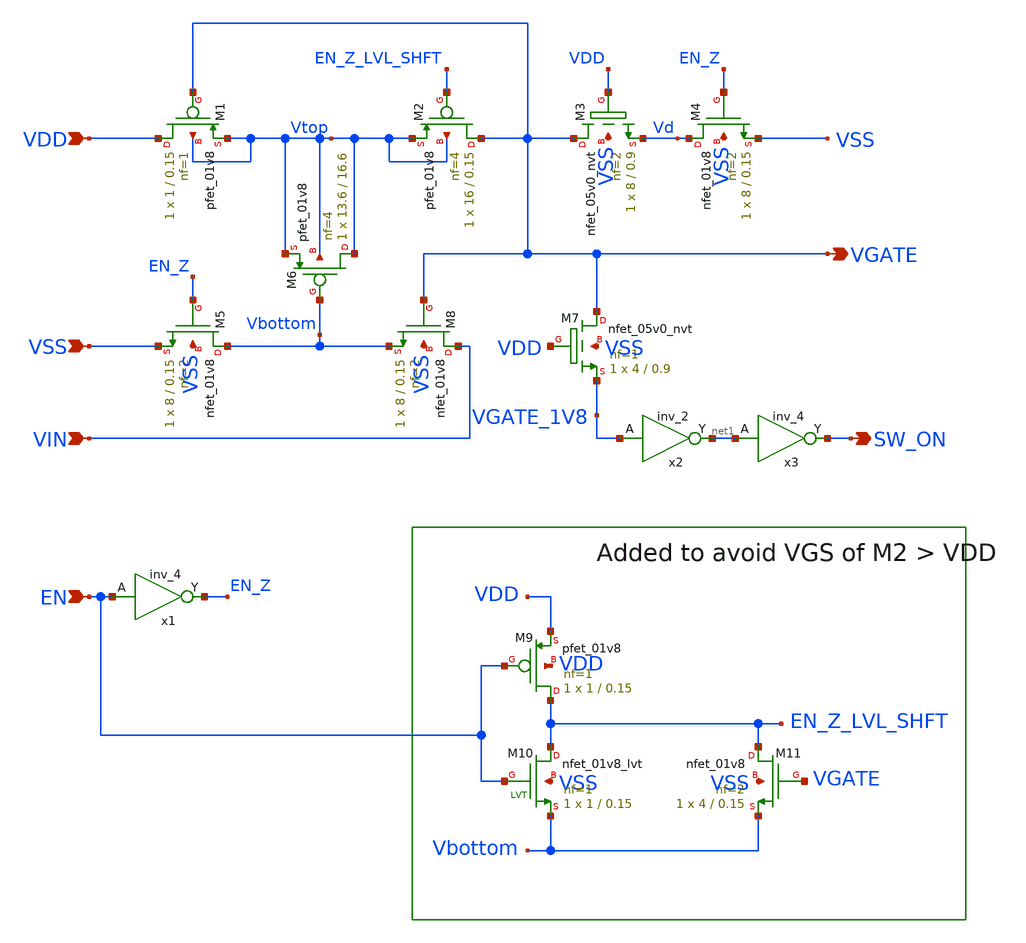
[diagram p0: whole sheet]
** sch_path: schematic/subcells/bootstrap/bootstrap.sch
**.subckt bootstrap VDD VSS VIN VGATE EN SW_ON
*.ipin VDD
*.ipin VSS
*.ipin VIN
*.opin VGATE
*.ipin EN
*.opin SW_ON
XM1 VDD VGATE Vtop Vtop sky130_fd_pr__pfet_01v8 L=0.15 W=1 nf=1 ad='int((nf+1)/2) * W/nf * 0.29' as='int((nf+2)/2) * W/nf * 0.29'
+ pd='2*int((nf+1)/2) * (W/nf + 0.29)' ps='2*int((nf+2)/2) * (W/nf + 0.29)' nrd='0.29 / W' nrs='0.29 / W'
+ sa=0 sb=0 sd=0 mult=1 m=1
XM2 VGATE EN_Z_LVL_SHFT Vtop Vtop sky130_fd_pr__pfet_01v8 L=0.15 W=16 nf=4 ad='int((nf+1)/2) * W/nf * 0.29'
+ as='int((nf+2)/2) * W/nf * 0.29' pd='2*int((nf+1)/2) * (W/nf + 0.29)' ps='2*int((nf+2)/2) * (W/nf + 0.29)'
+ nrd='0.29 / W' nrs='0.29 / W' sa=0 sb=0 sd=0 mult=1 m=1
XM3 VGATE VDD Vd VSS sky130_fd_pr__nfet_05v0_nvt L=0.9 W=8 nf=2 ad='int((nf+1)/2) * W/nf * 0.29' as='int((nf+2)/2) * W/nf * 0.29'
+ pd='2*int((nf+1)/2) * (W/nf + 0.29)' ps='2*int((nf+2)/2) * (W/nf + 0.29)' nrd='0.29 / W' nrs='0.29 / W'
+ sa=0 sb=0 sd=0 mult=1 m=1
XM4 Vd EN_Z VSS VSS sky130_fd_pr__nfet_01v8 L=0.15 W=8 nf=2 ad='int((nf+1)/2) * W/nf * 0.29' as='int((nf+2)/2) * W/nf * 0.29'
+ pd='2*int((nf+1)/2) * (W/nf + 0.29)' ps='2*int((nf+2)/2) * (W/nf + 0.29)' nrd='0.29 / W' nrs='0.29 / W'
+ sa=0 sb=0 sd=0 mult=1 m=1
XM5 Vbottom EN_Z VSS VSS sky130_fd_pr__nfet_01v8 L=0.15 W=8 nf=2 ad='int((nf+1)/2) * W/nf * 0.29' as='int((nf+2)/2) * W/nf * 0.29'
+ pd='2*int((nf+1)/2) * (W/nf + 0.29)' ps='2*int((nf+2)/2) * (W/nf + 0.29)' nrd='0.29 / W' nrs='0.29 / W'
+ sa=0 sb=0 sd=0 mult=1 m=1
XM6 Vtop Vbottom Vtop Vtop sky130_fd_pr__pfet_01v8 L=16.6 W=13.6 nf=4 ad='int((nf+1)/2) * W/nf * 0.29'
+ as='int((nf+2)/2) * W/nf * 0.29' pd='2*int((nf+1)/2) * (W/nf + 0.29)' ps='2*int((nf+2)/2) * (W/nf + 0.29)'
+ nrd='0.29 / W' nrs='0.29 / W' sa=0 sb=0 sd=0 mult=1 m=1
x1 EN VSS VSS VDD VDD EN_Z sky130_fd_sc_hd__inv_4
XM8 VIN VGATE Vbottom VSS sky130_fd_pr__nfet_01v8 L=0.15 W=8 nf=2 ad='int((nf+1)/2) * W/nf * 0.29' as='int((nf+2)/2) * W/nf * 0.29'
+ pd='2*int((nf+1)/2) * (W/nf + 0.29)' ps='2*int((nf+2)/2) * (W/nf + 0.29)' nrd='0.29 / W' nrs='0.29 / W'
+ sa=0 sb=0 sd=0 mult=1 m=1
XM7 VGATE VDD VGATE_1V8 VSS sky130_fd_pr__nfet_05v0_nvt L=0.9 W=4 nf=1 ad='int((nf+1)/2) * W/nf * 0.29'
+ as='int((nf+2)/2) * W/nf * 0.29' pd='2*int((nf+1)/2) * (W/nf + 0.29)' ps='2*int((nf+2)/2) * (W/nf + 0.29)'
+ nrd='0.29 / W' nrs='0.29 / W' sa=0 sb=0 sd=0 mult=1 m=1
x2 VGATE_1V8 VSS VSS VDD VDD net1 sky130_fd_sc_hd__inv_2
x3 net1 VSS VSS VDD VDD SW_ON sky130_fd_sc_hd__inv_4
XM9 EN_Z_LVL_SHFT EN VDD VDD sky130_fd_pr__pfet_01v8 L=0.15 W=1 nf=1 ad='int((nf+1)/2) * W/nf * 0.29'
+ as='int((nf+2)/2) * W/nf * 0.29' pd='2*int((nf+1)/2) * (W/nf + 0.29)' ps='2*int((nf+2)/2) * (W/nf + 0.29)'
+ nrd='0.29 / W' nrs='0.29 / W' sa=0 sb=0 sd=0 mult=1 m=1
XM10 EN_Z_LVL_SHFT EN Vbottom VSS sky130_fd_pr__nfet_01v8_lvt L=0.15 W=1 nf=1 ad='int((nf+1)/2) * W/nf * 0.29'
+ as='int((nf+2)/2) * W/nf * 0.29' pd='2*int((nf+1)/2) * (W/nf + 0.29)' ps='2*int((nf+2)/2) * (W/nf + 0.29)'
+ nrd='0.29 / W' nrs='0.29 / W' sa=0 sb=0 sd=0 mult=1 m=1
XM11 EN_Z_LVL_SHFT VGATE Vbottom VSS sky130_fd_pr__nfet_01v8 L=0.15 W=4 nf=2 ad='int((nf+1)/2) * W/nf * 0.29'
+ as='int((nf+2)/2) * W/nf * 0.29' pd='2*int((nf+1)/2) * (W/nf + 0.29)' ps='2*int((nf+2)/2) * (W/nf + 0.29)'
+ nrd='0.29 / W' nrs='0.29 / W' sa=0 sb=0 sd=0 mult=1 m=1
**.ends
.end
